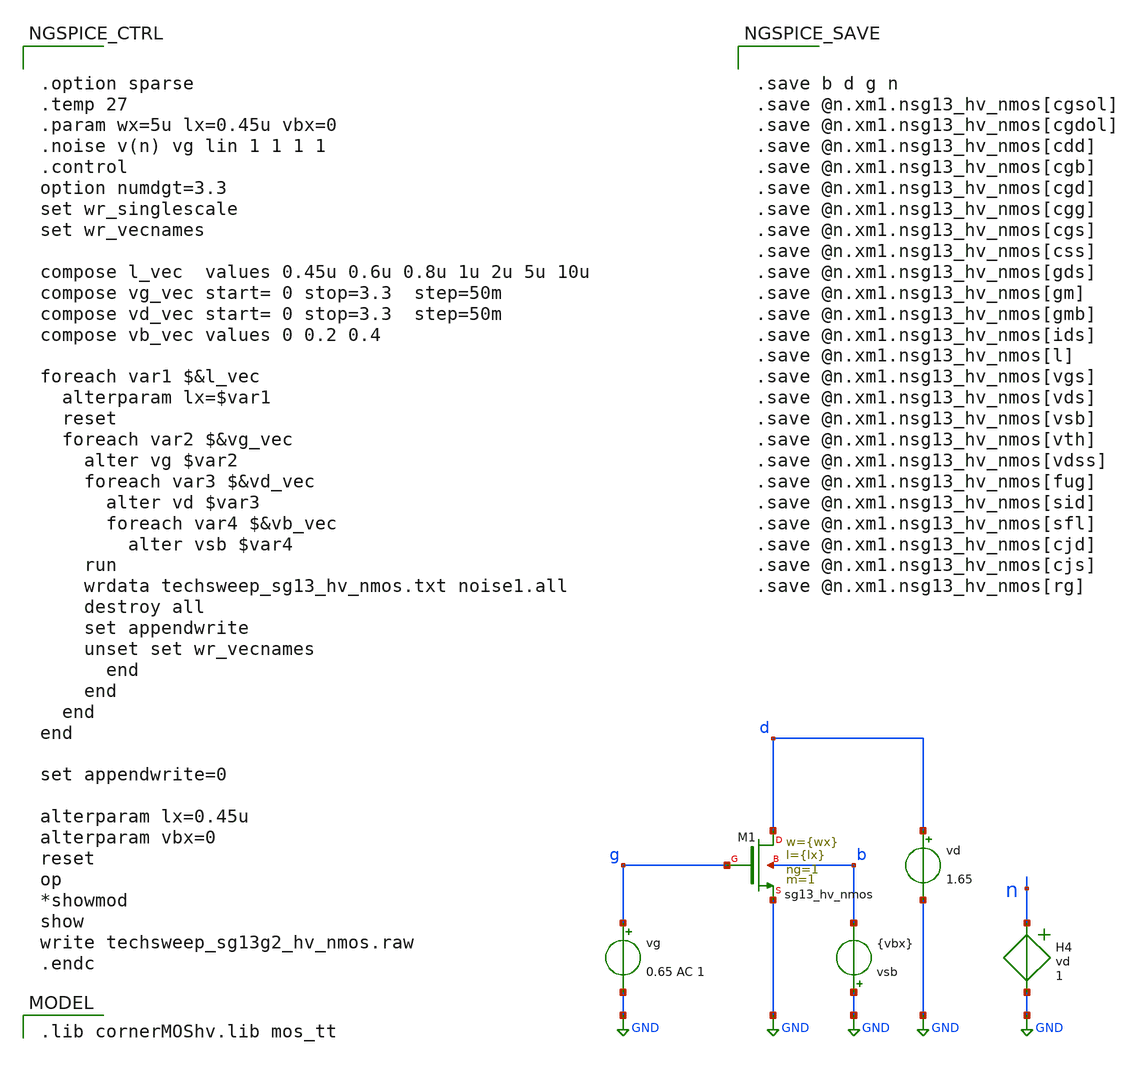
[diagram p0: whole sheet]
** sch_path: 3_real_circuits/techsweep_sg13g2_hv_nmos_test.sch
**.subckt techsweep_sg13g2_hv_nmos_test
vg g GND 0.65 AC 1
vd d GND 1.65
XM1 d g GND b sg13_hv_nmos w={wx} l={lx} ng=1 m=1 mm_ok=1
vsb GND b {vbx}
H4 n GND vd 1
**** begin user architecture code
 .lib cornerMOShv.lib mos_tt



.option sparse
.temp 27
.param wx=5u lx=0.45u vbx=0
.noise v(n) vg lin 1 1 1 1
.control
option numdgt=3.3
set wr_singlescale
set wr_vecnames

compose l_vec  values 0.45u 0.6u 0.8u 1u 2u 5u 10u
compose vg_vec start= 0 stop=3.3  step=50m
compose vd_vec start= 0 stop=3.3  step=50m
compose vb_vec values 0 0.2 0.4

foreach var1 $&l_vec
  alterparam lx=$var1
  reset
  foreach var2 $&vg_vec
    alter vg $var2
    foreach var3 $&vd_vec
      alter vd $var3
      foreach var4 $&vb_vec
        alter vsb $var4
	run
	wrdata techsweep_sg13_hv_nmos.txt noise1.all
	destroy all
	set appendwrite
	unset set wr_vecnames
      end
    end
  end
end

set appendwrite=0

alterparam lx=0.45u
alterparam vbx=0
reset
op
*showmod
show
write techsweep_sg13g2_hv_nmos.raw
.endc




.save b d g n
.save @n.xm1.nsg13_hv_nmos[cgsol]
.save @n.xm1.nsg13_hv_nmos[cgdol]
.save @n.xm1.nsg13_hv_nmos[cdd]
.save @n.xm1.nsg13_hv_nmos[cgb]
.save @n.xm1.nsg13_hv_nmos[cgd]
.save @n.xm1.nsg13_hv_nmos[cgg]
.save @n.xm1.nsg13_hv_nmos[cgs]
.save @n.xm1.nsg13_hv_nmos[css]
.save @n.xm1.nsg13_hv_nmos[gds]
.save @n.xm1.nsg13_hv_nmos[gm]
.save @n.xm1.nsg13_hv_nmos[gmb]
.save @n.xm1.nsg13_hv_nmos[ids]
.save @n.xm1.nsg13_hv_nmos[l]
.save @n.xm1.nsg13_hv_nmos[vgs]
.save @n.xm1.nsg13_hv_nmos[vds]
.save @n.xm1.nsg13_hv_nmos[vsb]
.save @n.xm1.nsg13_hv_nmos[vth]
.save @n.xm1.nsg13_hv_nmos[vdss]
.save @n.xm1.nsg13_hv_nmos[fug]
.save @n.xm1.nsg13_hv_nmos[sid]
.save @n.xm1.nsg13_hv_nmos[sfl]
.save @n.xm1.nsg13_hv_nmos[cjd]
.save @n.xm1.nsg13_hv_nmos[cjs]
.save @n.xm1.nsg13_hv_nmos[rg]


**** end user architecture code
**.ends
.GLOBAL GND
.end
